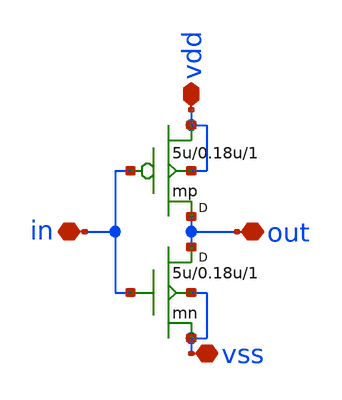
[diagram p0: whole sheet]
** sch_path: samples/digital_cosimulation/ainv/symbol/ainv.sch


.model p1 pmos   level=2 vto=-0.5 kp=8.5e-6 gamma=0.4 phi=0.65 lambda=0.05 xj=0.5e-6
.model n1 nmos   level=2 vto=0.5 kp=24e-6 gamma=0.15 phi=0.65 lambda=0.015 xj=0.5e-6


**.subckt ainv vdd out vss in
*.iopin vdd
*.iopin out
*.iopin vss
*.iopin in
mn out in vss vss n1 w=5u l=0.18u m=1
mp out in vdd vdd p1 w=5u l=0.18u m=1
**.ends
.end
